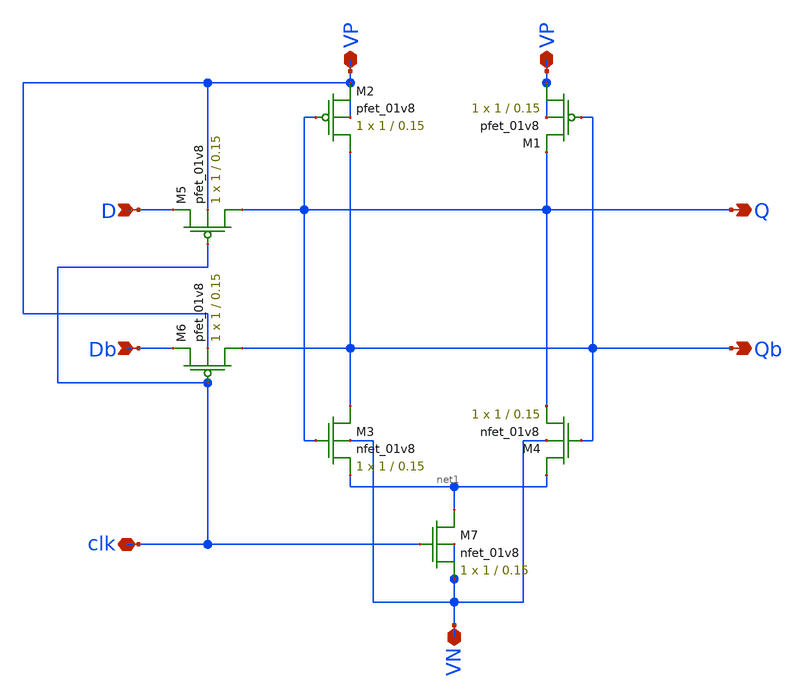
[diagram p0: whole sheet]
** sch_path: Mini_Project_2/CSRL/CSRL.sch
**.subckt CSRL D Db Q Qb clk VN VP VP
*.ipin D
*.ipin Db
*.opin Q
*.opin Qb
*.iopin clk
*.iopin VN
*.iopin VP
*.iopin VP
XM1 VP Qb Q VP sky130_fd_pr__pfet_01v8 L=0.15 W=1 nf=1 ad='int((nf+1)/2) * W/nf * 0.29' as='int((nf+2)/2) * W/nf * 0.29'
+ pd='2*int((nf+1)/2) * (W/nf + 0.29)' ps='2*int((nf+2)/2) * (W/nf + 0.29)' nrd='0.29 / W' nrs='0.29 / W'
+ sa=0 sb=0 sd=0 mult=1 m=1
XM2 Qb Q VP VP sky130_fd_pr__pfet_01v8 L=0.15 W=1 nf=1 ad='int((nf+1)/2) * W/nf * 0.29' as='int((nf+2)/2) * W/nf * 0.29'
+ pd='2*int((nf+1)/2) * (W/nf + 0.29)' ps='2*int((nf+2)/2) * (W/nf + 0.29)' nrd='0.29 / W' nrs='0.29 / W'
+ sa=0 sb=0 sd=0 mult=1 m=1
XM5 Q clk D VP sky130_fd_pr__pfet_01v8 L=0.15 W=1 nf=1 ad='int((nf+1)/2) * W/nf * 0.29' as='int((nf+2)/2) * W/nf * 0.29'
+ pd='2*int((nf+1)/2) * (W/nf + 0.29)' ps='2*int((nf+2)/2) * (W/nf + 0.29)' nrd='0.29 / W' nrs='0.29 / W'
+ sa=0 sb=0 sd=0 mult=1 m=1
XM6 Qb clk Db VP sky130_fd_pr__pfet_01v8 L=0.15 W=1 nf=1 ad='int((nf+1)/2) * W/nf * 0.29' as='int((nf+2)/2) * W/nf * 0.29'
+ pd='2*int((nf+1)/2) * (W/nf + 0.29)' ps='2*int((nf+2)/2) * (W/nf + 0.29)' nrd='0.29 / W' nrs='0.29 / W'
+ sa=0 sb=0 sd=0 mult=1 m=1
XM4 net1 Qb Q VN sky130_fd_pr__nfet_01v8 L=0.15 W=1 nf=1 ad='int((nf+1)/2) * W/nf * 0.29' as='int((nf+2)/2) * W/nf * 0.29'
+ pd='2*int((nf+1)/2) * (W/nf + 0.29)' ps='2*int((nf+2)/2) * (W/nf + 0.29)' nrd='0.29 / W' nrs='0.29 / W'
+ sa=0 sb=0 sd=0 mult=1 m=1
XM3 Qb Q net1 VN sky130_fd_pr__nfet_01v8 L=0.15 W=1 nf=1 ad='int((nf+1)/2) * W/nf * 0.29' as='int((nf+2)/2) * W/nf * 0.29'
+ pd='2*int((nf+1)/2) * (W/nf + 0.29)' ps='2*int((nf+2)/2) * (W/nf + 0.29)' nrd='0.29 / W' nrs='0.29 / W'
+ sa=0 sb=0 sd=0 mult=1 m=1
XM7 net1 clk VN VN sky130_fd_pr__nfet_01v8 L=0.15 W=1 nf=1 ad='int((nf+1)/2) * W/nf * 0.29' as='int((nf+2)/2) * W/nf * 0.29'
+ pd='2*int((nf+1)/2) * (W/nf + 0.29)' ps='2*int((nf+2)/2) * (W/nf + 0.29)' nrd='0.29 / W' nrs='0.29 / W'
+ sa=0 sb=0 sd=0 mult=1 m=1
**.ends
.end
